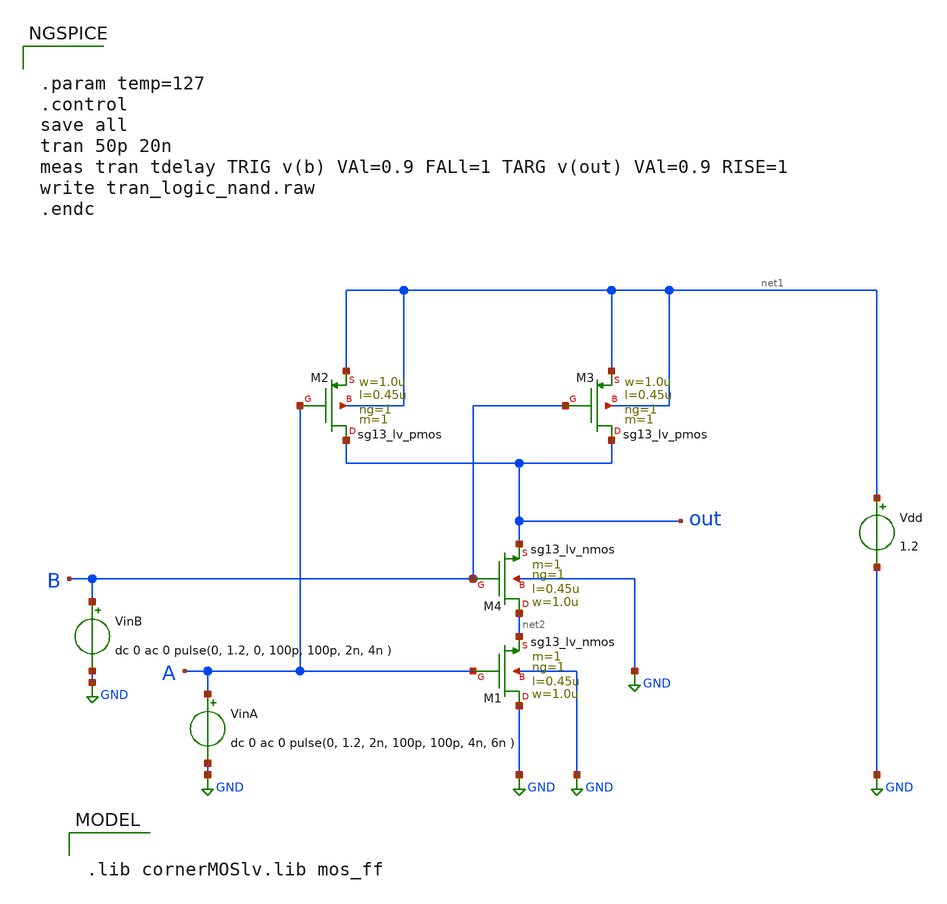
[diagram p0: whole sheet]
** sch_path: ihp-sg13g2/libs.tech/xschem/sg13g2_tests/tran_logic_nand.sch
* Copyright 2023 IHP PDK Authors
**.subckt tran_logic_nand
VinA A GND dc 0 ac 0 pulse(0, 1.2, 2n, 100p, 100p, 4n, 6n )
Vdd net1 GND 1.2
XM1 GND A net2 GND sg13_lv_nmos w=1.0u l=0.45u ng=1 m=1 mm_ok=1
XM2 out A net1 net1 sg13_lv_pmos w=1.0u l=0.45u ng=1 m=1 mm_ok=1
XM3 out B net1 net1 sg13_lv_pmos w=1.0u l=0.45u ng=1 m=1 mm_ok=1
XM4 net2 B out GND sg13_lv_nmos w=1.0u l=0.45u ng=1 m=1 mm_ok=1
VinB B GND dc 0 ac 0 pulse(0, 1.2, 0, 100p, 100p, 2n, 4n )
**** begin user architecture code

.lib cornerMOSlv.lib mos_ff



.param temp=127
.control
save all
tran 50p 20n
meas tran tdelay TRIG v(b) VAl=0.9 FALl=1 TARG v(out) VAl=0.9 RISE=1
write tran_logic_nand.raw
.endc


**** end user architecture code
**.ends
.GLOBAL GND
.end
